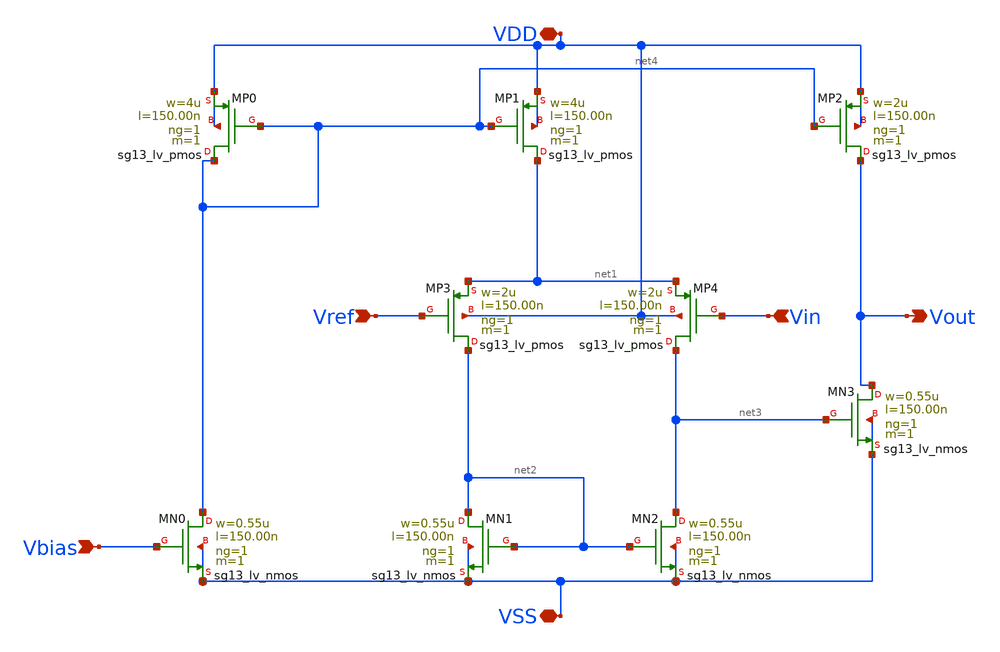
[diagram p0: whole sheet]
** sch_path: schematic/OpampVEdu.sch
**.subckt OpampVEdu Vin VDD VSS Vref Vout Vbias
*.ipin Vin
*.iopin VDD
*.iopin VSS
*.ipin Vref
*.opin Vout
*.ipin Vbias
XMP0 net4 net4 VDD VDD sg13_lv_pmos w=4u l=150.00n ng=1 m=1 mm_ok=1
XMN2 net3 net2 VSS VSS sg13_lv_nmos w=0.55u l=150.00n ng=1 m=1 mm_ok=1
XMN1 net2 net2 VSS VSS sg13_lv_nmos w=0.55u l=150.00n ng=1 m=1 mm_ok=1
XMN0 net4 Vbias VSS VSS sg13_lv_nmos w=0.55u l=150.00n ng=1 m=1 mm_ok=1
XMP4 net3 Vin net1 VDD sg13_lv_pmos w=2u l=150.00n ng=1 m=1 mm_ok=1
XMP3 net2 Vref net1 VDD sg13_lv_pmos w=2u l=150.00n ng=1 m=1 mm_ok=1
XMP1 net1 net4 VDD VDD sg13_lv_pmos w=4u l=150.00n ng=1 m=1 mm_ok=1
XMP2 Vout net4 VDD VDD sg13_lv_pmos w=2u l=150.00n ng=1 m=1 mm_ok=1
XMN3 Vout net3 VSS VSS sg13_lv_nmos w=0.55u l=150.00n ng=1 m=1 mm_ok=1
**.ends
.end
